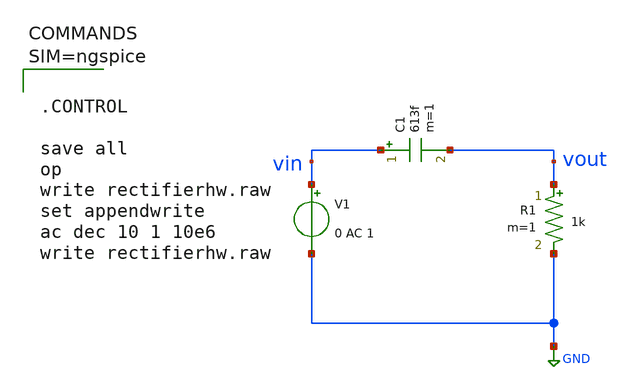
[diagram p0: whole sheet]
** sch_path: work/xschem/rectifierhw.sch
**.subckt rectifierhw
V1 vin GND 0 AC 1
C1 vin vout 613f m=1
R1 vout GND 1k m=1
**** begin user architecture code



.CONTROL

save all
op
write rectifierhw.raw
set appendwrite
ac dec 10 1 10e6
write rectifierhw.raw




**** end user architecture code
**.ends
.GLOBAL GND
.end
